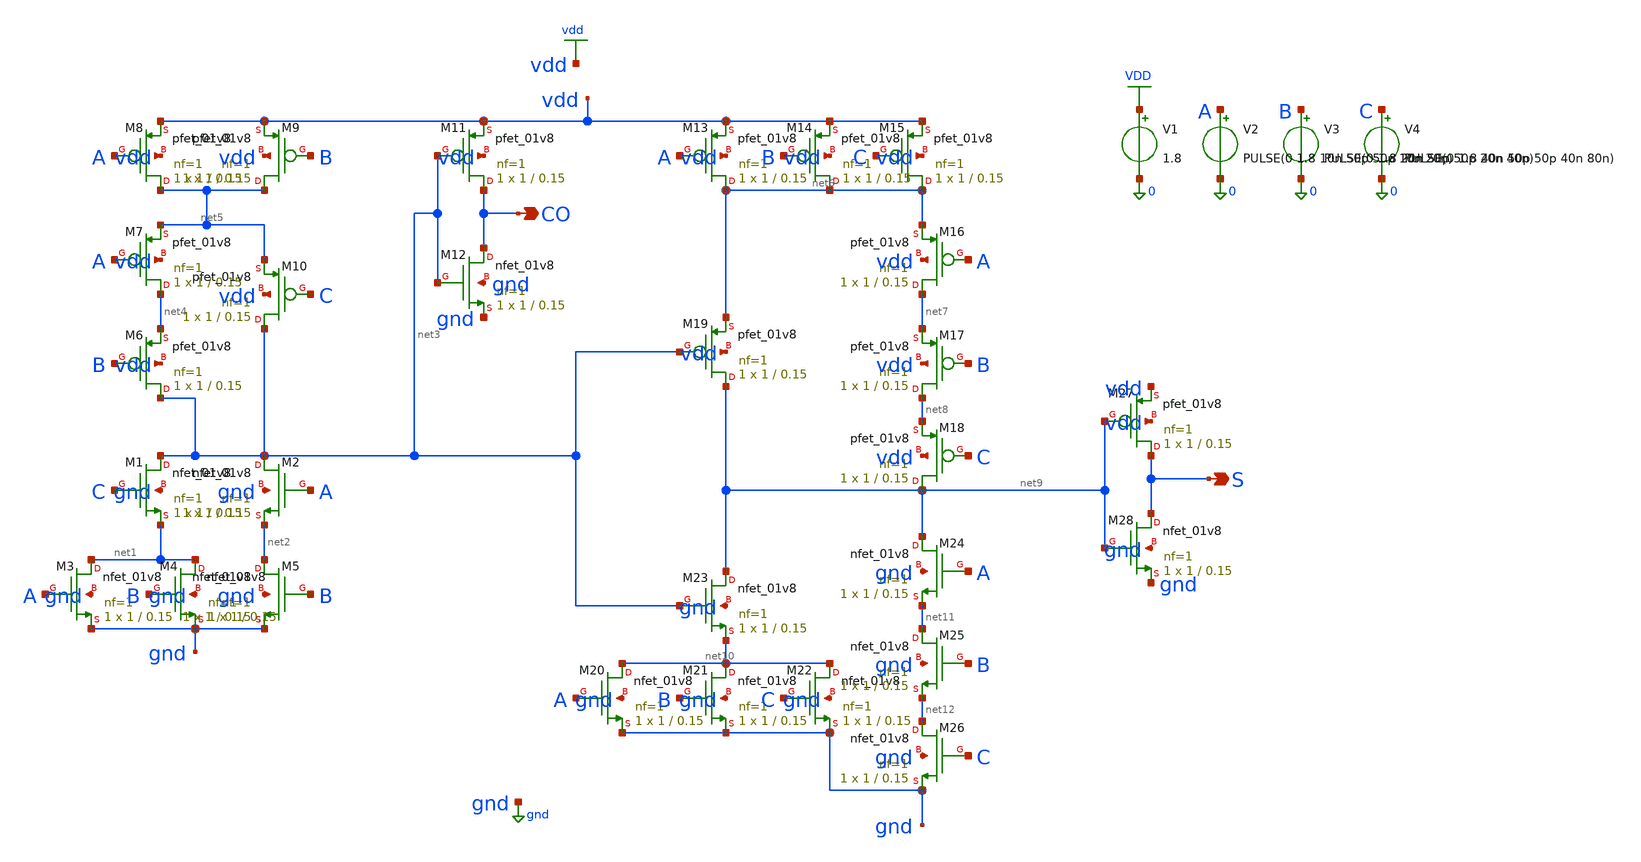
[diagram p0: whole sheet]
** sch_path: tb_fulladder1bit.sch
**.subckt tb_fulladder1bit CO S
*.opin CO
*.opin S
XM1 net3 C net1 gnd sky130_fd_pr__nfet_01v8 L=0.15 W=1 nf=1 ad='int((1 + 1)/2) * 1 / 1 * 0.29' as='int((1 + 2)/2) * 1 / 1 * 0.29'
+ pd='2*int((1 + 1)/2) * (1 / 1 + 0.29)' ps='2*int((1 + 2)/2) * (1 / 1 + 0.29)' nrd='0.29 / 1 ' nrs='0.29 / 1 '
+ sa=0 sb=0 sd=0 mult=1 m=1
XM2 net3 A net2 gnd sky130_fd_pr__nfet_01v8 L=0.15 W=1 nf=1 ad='int((1 + 1)/2) * 1 / 1 * 0.29' as='int((1 + 2)/2) * 1 / 1 * 0.29'
+ pd='2*int((1 + 1)/2) * (1 / 1 + 0.29)' ps='2*int((1 + 2)/2) * (1 / 1 + 0.29)' nrd='0.29 / 1 ' nrs='0.29 / 1 '
+ sa=0 sb=0 sd=0 mult=1 m=1
XM3 net1 A gnd gnd sky130_fd_pr__nfet_01v8 L=0.15 W=1 nf=1 ad='int((1 + 1)/2) * 1 / 1 * 0.29' as='int((1 + 2)/2) * 1 / 1 * 0.29'
+ pd='2*int((1 + 1)/2) * (1 / 1 + 0.29)' ps='2*int((1 + 2)/2) * (1 / 1 + 0.29)' nrd='0.29 / 1 ' nrs='0.29 / 1 '
+ sa=0 sb=0 sd=0 mult=1 m=1
XM4 net1 B gnd gnd sky130_fd_pr__nfet_01v8 L=0.15 W=1 nf=1 ad='int((1 + 1)/2) * 1 / 1 * 0.29' as='int((1 + 2)/2) * 1 / 1 * 0.29'
+ pd='2*int((1 + 1)/2) * (1 / 1 + 0.29)' ps='2*int((1 + 2)/2) * (1 / 1 + 0.29)' nrd='0.29 / 1 ' nrs='0.29 / 1 '
+ sa=0 sb=0 sd=0 mult=1 m=1
XM5 net2 B gnd gnd sky130_fd_pr__nfet_01v8 L=0.15 W=1 nf=1 ad='int((1 + 1)/2) * 1 / 1 * 0.29' as='int((1 + 2)/2) * 1 / 1 * 0.29'
+ pd='2*int((1 + 1)/2) * (1 / 1 + 0.29)' ps='2*int((1 + 2)/2) * (1 / 1 + 0.29)' nrd='0.29 / 1 ' nrs='0.29 / 1 '
+ sa=0 sb=0 sd=0 mult=1 m=1
XM6 net3 B net4 vdd sky130_fd_pr__pfet_01v8 L=0.15 W=1 nf=1 ad='int((1 + 1)/2) * 1 / 1 * 0.29' as='int((1 + 2)/2) * 1 / 1 * 0.29'
+ pd='2*int((1 + 1)/2) * (1 / 1 + 0.29)' ps='2*int((1 + 2)/2) * (1 / 1 + 0.29)' nrd='0.29 / 1 ' nrs='0.29 / 1 '
+ sa=0 sb=0 sd=0 mult=1 m=1
XM7 net4 A net5 vdd sky130_fd_pr__pfet_01v8 L=0.15 W=1 nf=1 ad='int((1 + 1)/2) * 1 / 1 * 0.29' as='int((1 + 2)/2) * 1 / 1 * 0.29'
+ pd='2*int((1 + 1)/2) * (1 / 1 + 0.29)' ps='2*int((1 + 2)/2) * (1 / 1 + 0.29)' nrd='0.29 / 1 ' nrs='0.29 / 1 '
+ sa=0 sb=0 sd=0 mult=1 m=1
XM8 net5 A vdd vdd sky130_fd_pr__pfet_01v8 L=0.15 W=1 nf=1 ad='int((1 + 1)/2) * 1 / 1 * 0.29' as='int((1 + 2)/2) * 1 / 1 * 0.29'
+ pd='2*int((1 + 1)/2) * (1 / 1 + 0.29)' ps='2*int((1 + 2)/2) * (1 / 1 + 0.29)' nrd='0.29 / 1 ' nrs='0.29 / 1 '
+ sa=0 sb=0 sd=0 mult=1 m=1
XM9 net5 B vdd vdd sky130_fd_pr__pfet_01v8 L=0.15 W=1 nf=1 ad='int((1 + 1)/2) * 1 / 1 * 0.29' as='int((1 + 2)/2) * 1 / 1 * 0.29'
+ pd='2*int((1 + 1)/2) * (1 / 1 + 0.29)' ps='2*int((1 + 2)/2) * (1 / 1 + 0.29)' nrd='0.29 / 1 ' nrs='0.29 / 1 '
+ sa=0 sb=0 sd=0 mult=1 m=1
XM10 net3 C net5 vdd sky130_fd_pr__pfet_01v8 L=0.15 W=1 nf=1 ad='int((1 + 1)/2) * 1 / 1 * 0.29' as='int((1 + 2)/2) * 1 / 1 * 0.29'
+ pd='2*int((1 + 1)/2) * (1 / 1 + 0.29)' ps='2*int((1 + 2)/2) * (1 / 1 + 0.29)' nrd='0.29 / 1 ' nrs='0.29 / 1 '
+ sa=0 sb=0 sd=0 mult=1 m=1
XM11 CO net3 vdd vdd sky130_fd_pr__pfet_01v8 L=0.15 W=1 nf=1 ad='int((1 + 1)/2) * 1 / 1 * 0.29' as='int((1 + 2)/2) * 1 / 1 * 0.29'
+ pd='2*int((1 + 1)/2) * (1 / 1 + 0.29)' ps='2*int((1 + 2)/2) * (1 / 1 + 0.29)' nrd='0.29 / 1 ' nrs='0.29 / 1 '
+ sa=0 sb=0 sd=0 mult=1 m=1
XM12 CO net3 gnd gnd sky130_fd_pr__nfet_01v8 L=0.15 W=1 nf=1 ad='int((1 + 1)/2) * 1 / 1 * 0.29' as='int((1 + 2)/2) * 1 / 1 * 0.29'
+ pd='2*int((1 + 1)/2) * (1 / 1 + 0.29)' ps='2*int((1 + 2)/2) * (1 / 1 + 0.29)' nrd='0.29 / 1 ' nrs='0.29 / 1 '
+ sa=0 sb=0 sd=0 mult=1 m=1
XM13 net6 A vdd vdd sky130_fd_pr__pfet_01v8 L=0.15 W=1 nf=1 ad='int((1 + 1)/2) * 1 / 1 * 0.29' as='int((1 + 2)/2) * 1 / 1 * 0.29'
+ pd='2*int((1 + 1)/2) * (1 / 1 + 0.29)' ps='2*int((1 + 2)/2) * (1 / 1 + 0.29)' nrd='0.29 / 1 ' nrs='0.29 / 1 '
+ sa=0 sb=0 sd=0 mult=1 m=1
XM14 net6 B vdd vdd sky130_fd_pr__pfet_01v8 L=0.15 W=1 nf=1 ad='int((1 + 1)/2) * 1 / 1 * 0.29' as='int((1 + 2)/2) * 1 / 1 * 0.29'
+ pd='2*int((1 + 1)/2) * (1 / 1 + 0.29)' ps='2*int((1 + 2)/2) * (1 / 1 + 0.29)' nrd='0.29 / 1 ' nrs='0.29 / 1 '
+ sa=0 sb=0 sd=0 mult=1 m=1
XM15 net6 C vdd vdd sky130_fd_pr__pfet_01v8 L=0.15 W=1 nf=1 ad='int((1 + 1)/2) * 1 / 1 * 0.29' as='int((1 + 2)/2) * 1 / 1 * 0.29'
+ pd='2*int((1 + 1)/2) * (1 / 1 + 0.29)' ps='2*int((1 + 2)/2) * (1 / 1 + 0.29)' nrd='0.29 / 1 ' nrs='0.29 / 1 '
+ sa=0 sb=0 sd=0 mult=1 m=1
XM16 net7 A net6 vdd sky130_fd_pr__pfet_01v8 L=0.15 W=1 nf=1 ad='int((1 + 1)/2) * 1 / 1 * 0.29' as='int((1 + 2)/2) * 1 / 1 * 0.29'
+ pd='2*int((1 + 1)/2) * (1 / 1 + 0.29)' ps='2*int((1 + 2)/2) * (1 / 1 + 0.29)' nrd='0.29 / 1 ' nrs='0.29 / 1 '
+ sa=0 sb=0 sd=0 mult=1 m=1
XM17 net8 B net7 vdd sky130_fd_pr__pfet_01v8 L=0.15 W=1 nf=1 ad='int((1 + 1)/2) * 1 / 1 * 0.29' as='int((1 + 2)/2) * 1 / 1 * 0.29'
+ pd='2*int((1 + 1)/2) * (1 / 1 + 0.29)' ps='2*int((1 + 2)/2) * (1 / 1 + 0.29)' nrd='0.29 / 1 ' nrs='0.29 / 1 '
+ sa=0 sb=0 sd=0 mult=1 m=1
XM18 net9 C net8 vdd sky130_fd_pr__pfet_01v8 L=0.15 W=1 nf=1 ad='int((1 + 1)/2) * 1 / 1 * 0.29' as='int((1 + 2)/2) * 1 / 1 * 0.29'
+ pd='2*int((1 + 1)/2) * (1 / 1 + 0.29)' ps='2*int((1 + 2)/2) * (1 / 1 + 0.29)' nrd='0.29 / 1 ' nrs='0.29 / 1 '
+ sa=0 sb=0 sd=0 mult=1 m=1
XM19 net9 net3 net6 vdd sky130_fd_pr__pfet_01v8 L=0.15 W=1 nf=1 ad='int((1 + 1)/2) * 1 / 1 * 0.29' as='int((1 + 2)/2) * 1 / 1 * 0.29'
+ pd='2*int((1 + 1)/2) * (1 / 1 + 0.29)' ps='2*int((1 + 2)/2) * (1 / 1 + 0.29)' nrd='0.29 / 1 ' nrs='0.29 / 1 '
+ sa=0 sb=0 sd=0 mult=1 m=1
XM20 net10 A gnd gnd sky130_fd_pr__nfet_01v8 L=0.15 W=1 nf=1 ad='int((1 + 1)/2) * 1 / 1 * 0.29' as='int((1 + 2)/2) * 1 / 1 * 0.29'
+ pd='2*int((1 + 1)/2) * (1 / 1 + 0.29)' ps='2*int((1 + 2)/2) * (1 / 1 + 0.29)' nrd='0.29 / 1 ' nrs='0.29 / 1 '
+ sa=0 sb=0 sd=0 mult=1 m=1
XM21 net10 B gnd gnd sky130_fd_pr__nfet_01v8 L=0.15 W=1 nf=1 ad='int((1 + 1)/2) * 1 / 1 * 0.29' as='int((1 + 2)/2) * 1 / 1 * 0.29'
+ pd='2*int((1 + 1)/2) * (1 / 1 + 0.29)' ps='2*int((1 + 2)/2) * (1 / 1 + 0.29)' nrd='0.29 / 1 ' nrs='0.29 / 1 '
+ sa=0 sb=0 sd=0 mult=1 m=1
XM22 net10 C gnd gnd sky130_fd_pr__nfet_01v8 L=0.15 W=1 nf=1 ad='int((1 + 1)/2) * 1 / 1 * 0.29' as='int((1 + 2)/2) * 1 / 1 * 0.29'
+ pd='2*int((1 + 1)/2) * (1 / 1 + 0.29)' ps='2*int((1 + 2)/2) * (1 / 1 + 0.29)' nrd='0.29 / 1 ' nrs='0.29 / 1 '
+ sa=0 sb=0 sd=0 mult=1 m=1
XM23 net9 net3 net10 gnd sky130_fd_pr__nfet_01v8 L=0.15 W=1 nf=1 ad='int((1 + 1)/2) * 1 / 1 * 0.29' as='int((1 + 2)/2) * 1 / 1 * 0.29'
+ pd='2*int((1 + 1)/2) * (1 / 1 + 0.29)' ps='2*int((1 + 2)/2) * (1 / 1 + 0.29)' nrd='0.29 / 1 ' nrs='0.29 / 1 '
+ sa=0 sb=0 sd=0 mult=1 m=1
XM24 net9 A net11 gnd sky130_fd_pr__nfet_01v8 L=0.15 W=1 nf=1 ad='int((1 + 1)/2) * 1 / 1 * 0.29' as='int((1 + 2)/2) * 1 / 1 * 0.29'
+ pd='2*int((1 + 1)/2) * (1 / 1 + 0.29)' ps='2*int((1 + 2)/2) * (1 / 1 + 0.29)' nrd='0.29 / 1 ' nrs='0.29 / 1 '
+ sa=0 sb=0 sd=0 mult=1 m=1
XM25 net11 B net12 gnd sky130_fd_pr__nfet_01v8 L=0.15 W=1 nf=1 ad='int((1 + 1)/2) * 1 / 1 * 0.29' as='int((1 + 2)/2) * 1 / 1 * 0.29'
+ pd='2*int((1 + 1)/2) * (1 / 1 + 0.29)' ps='2*int((1 + 2)/2) * (1 / 1 + 0.29)' nrd='0.29 / 1 ' nrs='0.29 / 1 '
+ sa=0 sb=0 sd=0 mult=1 m=1
XM26 net12 C gnd gnd sky130_fd_pr__nfet_01v8 L=0.15 W=1 nf=1 ad='int((1 + 1)/2) * 1 / 1 * 0.29' as='int((1 + 2)/2) * 1 / 1 * 0.29'
+ pd='2*int((1 + 1)/2) * (1 / 1 + 0.29)' ps='2*int((1 + 2)/2) * (1 / 1 + 0.29)' nrd='0.29 / 1 ' nrs='0.29 / 1 '
+ sa=0 sb=0 sd=0 mult=1 m=1
XM27 S net9 vdd vdd sky130_fd_pr__pfet_01v8 L=0.15 W=1 nf=1 ad='int((1 + 1)/2) * 1 / 1 * 0.29' as='int((1 + 2)/2) * 1 / 1 * 0.29'
+ pd='2*int((1 + 1)/2) * (1 / 1 + 0.29)' ps='2*int((1 + 2)/2) * (1 / 1 + 0.29)' nrd='0.29 / 1 ' nrs='0.29 / 1 '
+ sa=0 sb=0 sd=0 mult=1 m=1
XM28 S net9 gnd gnd sky130_fd_pr__nfet_01v8 L=0.15 W=1 nf=1 ad='int((1 + 1)/2) * 1 / 1 * 0.29' as='int((1 + 2)/2) * 1 / 1 * 0.29'
+ pd='2*int((1 + 1)/2) * (1 / 1 + 0.29)' ps='2*int((1 + 2)/2) * (1 / 1 + 0.29)' nrd='0.29 / 1 ' nrs='0.29 / 1 '
+ sa=0 sb=0 sd=0 mult=1 m=1
V1 VDD 0 1.8
V2 A 0 PULSE(0 1.8 10n 50p 50p 10n 20n)
V3 B 0 PULSE(0 1.8 20n 50p 50p 20n 40n)
V4 C 0 PULSE(0 1.8 40n 50p 50p 40n 80n)
**** begin user architecture code
.lib /foss/pdks/sky130A/libs.tech/ngspice/sky130.lib.spice tt

.control
save all
tran 50p 80n

plot v(A) v(B) v(C)
plot v(S) v(C0)
write /foss/designs/tb_fulladder1bit.raw
.endc

.end

**** end user architecture code
**.ends
.GLOBAL vdd
.GLOBAL gnd
.GLOBAL VDD
.end
